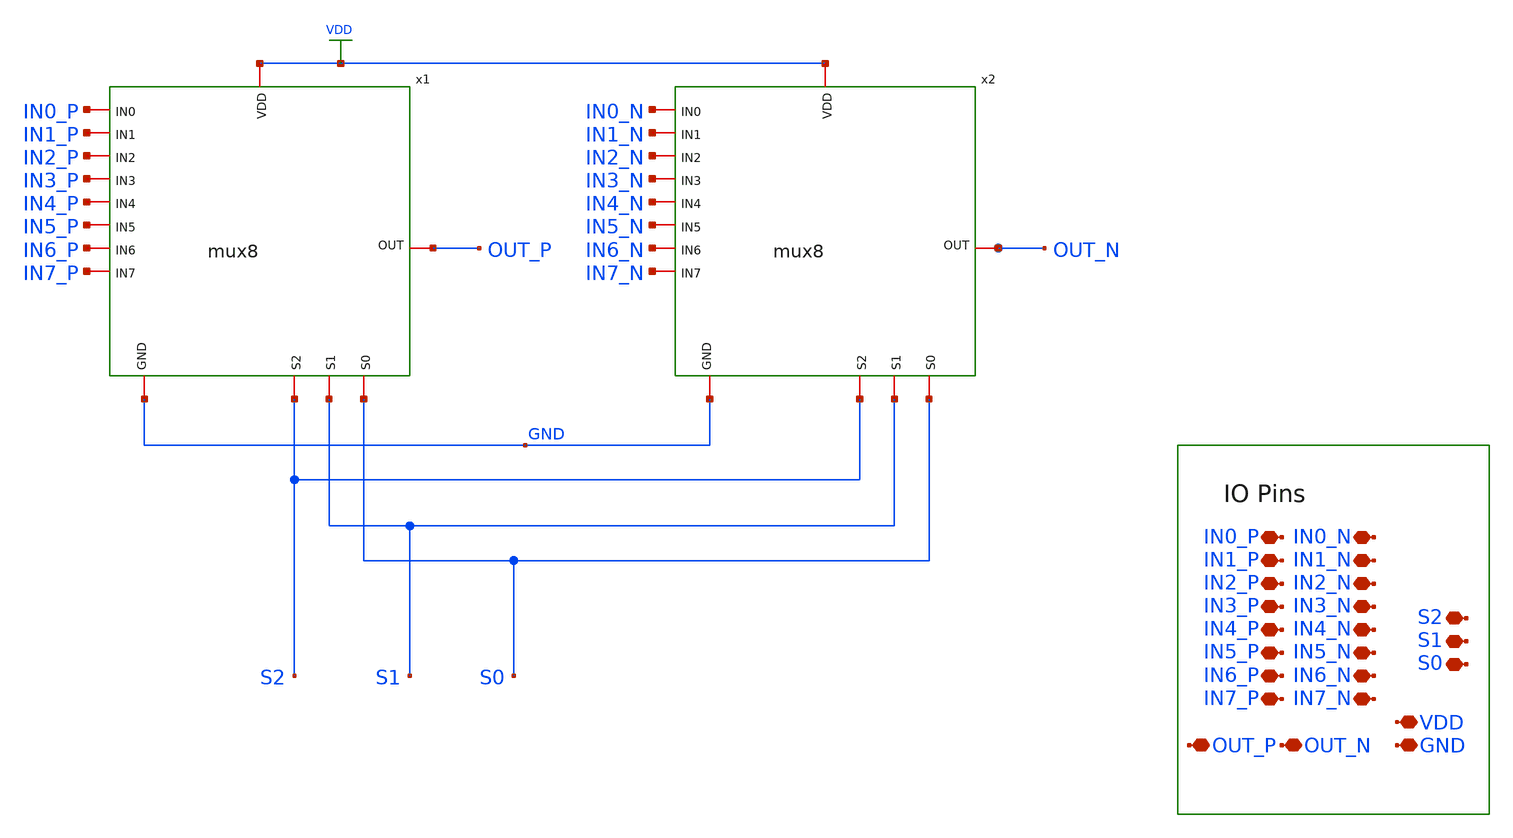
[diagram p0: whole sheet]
** sch_path: scope_sky130_v1/osc_input_mux.sch
**.subckt osc_input_mux IN1_P VDD GND IN2_P IN3_P IN4_P IN5_P IN6_P IN7_P IN0_P S2 S1 S0 OUT_P OUT_N
*+ IN1_N IN2_N IN3_N IN4_N IN5_N IN6_N IN7_N IN0_N
*.iopin IN1_P
*.iopin VDD
*.iopin GND
*.iopin IN2_P
*.iopin IN3_P
*.iopin IN4_P
*.iopin IN5_P
*.iopin IN6_P
*.iopin IN7_P
*.iopin IN0_P
*.iopin S2
*.iopin S1
*.iopin S0
*.iopin OUT_P
*.iopin OUT_N
*.iopin IN1_N
*.iopin IN2_N
*.iopin IN3_N
*.iopin IN4_N
*.iopin IN5_N
*.iopin IN6_N
*.iopin IN7_N
*.iopin IN0_N
x1 IN1_P IN2_P IN3_P IN4_P IN5_P IN6_P OUT_P IN7_P IN0_P S1 VDD S2 GND S0 mux8
x2 IN1_N IN2_N IN3_N IN4_N IN5_N IN6_N OUT_N IN7_N IN0_N S1 VDD S2 GND S0 mux8
**.ends

* expanding   symbol:  scope_sky130_v1/mux8.sym # of pins=14
** sym_path: scope_sky130_v1/mux8.sym
** sch_path: scope_sky130_v1/mux8.sch
.subckt mux8 IN1 IN2 IN3 IN4 IN5 IN6 OUT IN7 IN0 S1 VDD S2 GND S0
*.iopin IN3
*.iopin VDD
*.iopin GND
*.iopin S0
*.iopin OUT
*.iopin IN2
*.iopin IN1
*.iopin IN0
*.iopin S1
*.iopin IN7
*.iopin IN6
*.iopin IN5
*.iopin IN4
*.iopin S2
XM1 Sb S0 VDD VDD sky130_fd_pr__pfet_01v8_lvt L=0.35 W=1 nf=1 ad='int((1 + 1)/2) * 1 / 1 * 0.29' as='int((1 + 2)/2) * 1 / 1 * 0.29'
+ pd='2*int((1 + 1)/2) * (1 / 1 + 0.29)' ps='2*int((1 + 2)/2) * (1 / 1 + 0.29)' nrd='0.29 / 1 ' nrs='0.29 / 1 '
+ sa=0 sb=0 sd=0 mult=1 m=1
XM2 Sb S0 GND GND sky130_fd_pr__nfet_01v8_lvt L=0.15 W=1 nf=1 ad='int((1 + 1)/2) * 1 / 1 * 0.29' as='int((1 + 2)/2) * 1 / 1 * 0.29'
+ pd='2*int((1 + 1)/2) * (1 / 1 + 0.29)' ps='2*int((1 + 2)/2) * (1 / 1 + 0.29)' nrd='0.29 / 1 ' nrs='0.29 / 1 '
+ sa=0 sb=0 sd=0 mult=1 m=1
x1 IN7 net1 net5 S0 VDD GND tgate
x2 IN6 net1 net6 net5 VDD GND tgate
x3 IN5 net2 net5 net6 VDD GND tgate
x4 IN4 net2 S0 net5 VDD GND tgate
x5 IN3 net3 Sb S0 VDD GND tgate
x6 IN2 net3 S0 Sb VDD GND tgate
x7 IN1 net4 Sb S0 VDD GND tgate
x8 IN0 net4 S0 Sb VDD GND tgate
x9 net2 net1 S1 S2 net4 net3 OUT VDD GND mux4
.ends


* expanding   symbol:  scope_sky130_v1/tgate.sym # of pins=6
** sym_path: scope_sky130_v1/tgate.sym
** sch_path: scope_sky130_v1/tgate.sch
.subckt tgate IN OUT ENb EN VDD GND
*.iopin IN
*.iopin VDD
*.iopin GND
*.iopin ENb
*.iopin EN
*.iopin OUT
XM2 IN EN OUT GND sky130_fd_pr__nfet_01v8 L=0.15 W=0.5 nf=1 ad='int((1 + 1)/2) * 0.5 / 1 * 0.29' as='int((1 + 2)/2) * 0.5 / 1 * 0.29'
+ pd='2*int((1 + 1)/2) * (0.5 / 1 + 0.29)' ps='2*int((1 + 2)/2) * (0.5 / 1 + 0.29)' nrd='0.29 / 0.5 ' nrs='0.29 / 0.5 '
+ sa=0 sb=0 sd=0 mult=1 m=1
XM11 IN ENb OUT VDD sky130_fd_pr__pfet_01v8 L=0.15 W=0.5 nf=1 ad='int((nf+1)/2) * W/nf * 0.29' as='int((nf+2)/2) * W/nf * 0.29'
+ pd='2*int((nf+1)/2) * (W/nf + 0.29)' ps='2*int((nf+2)/2) * (W/nf + 0.29)' nrd='0.29 / W' nrs='0.29 / W'
+ sa=0 sb=0 sd=0 mult=1 m=1
.ends


* expanding   symbol:  scope_sky130_v1/mux4.sym # of pins=9
** sym_path: scope_sky130_v1/mux4.sym
** sch_path: scope_sky130_v1/mux4.sch
.subckt mux4 IN2 IN3 S0 S1 IN0 IN1 OUT VDD GND
*.iopin IN3
*.iopin VDD
*.iopin GND
*.iopin S0
*.iopin OUT
*.iopin IN2
*.iopin IN1
*.iopin IN0
*.iopin S1
XM1 Sb S0 VDD VDD sky130_fd_pr__pfet_01v8_lvt L=0.35 W=1 nf=1 ad='int((1 + 1)/2) * 1 / 1 * 0.29' as='int((1 + 2)/2) * 1 / 1 * 0.29'
+ pd='2*int((1 + 1)/2) * (1 / 1 + 0.29)' ps='2*int((1 + 2)/2) * (1 / 1 + 0.29)' nrd='0.29 / 1 ' nrs='0.29 / 1 '
+ sa=0 sb=0 sd=0 mult=1 m=1
XM2 Sb S0 GND GND sky130_fd_pr__nfet_01v8_lvt L=0.15 W=1 nf=1 ad='int((1 + 1)/2) * 1 / 1 * 0.29' as='int((1 + 2)/2) * 1 / 1 * 0.29'
+ pd='2*int((1 + 1)/2) * (1 / 1 + 0.29)' ps='2*int((1 + 2)/2) * (1 / 1 + 0.29)' nrd='0.29 / 1 ' nrs='0.29 / 1 '
+ sa=0 sb=0 sd=0 mult=1 m=1
x1 IN3 net1 Sb S0 VDD GND tgate
x2 IN2 net1 S0 Sb VDD GND tgate
x3 IN1 net2 Sb S0 VDD GND tgate
x4 IN0 net2 S0 Sb VDD GND tgate
x5 net2 net1 S1 OUT VDD GND mux2
.ends


* expanding   symbol:  scope_sky130_v1/mux2.sym # of pins=6
** sym_path: scope_sky130_v1/mux2.sym
** sch_path: scope_sky130_v1/mux2.sch
.subckt mux2 IN0 IN1 S OUT VDD GND
*.iopin IN1
*.iopin VDD
*.iopin GND
*.iopin S
*.iopin OUT
*.iopin IN0
XM1 Sb S VDD VDD sky130_fd_pr__pfet_01v8_lvt L=0.35 W=1 nf=1 ad='int((1 + 1)/2) * 1 / 1 * 0.29' as='int((1 + 2)/2) * 1 / 1 * 0.29'
+ pd='2*int((1 + 1)/2) * (1 / 1 + 0.29)' ps='2*int((1 + 2)/2) * (1 / 1 + 0.29)' nrd='0.29 / 1 ' nrs='0.29 / 1 '
+ sa=0 sb=0 sd=0 mult=1 m=1
XM2 Sb S GND GND sky130_fd_pr__nfet_01v8_lvt L=0.15 W=1 nf=1 ad='int((1 + 1)/2) * 1 / 1 * 0.29' as='int((1 + 2)/2) * 1 / 1 * 0.29'
+ pd='2*int((1 + 1)/2) * (1 / 1 + 0.29)' ps='2*int((1 + 2)/2) * (1 / 1 + 0.29)' nrd='0.29 / 1 ' nrs='0.29 / 1 '
+ sa=0 sb=0 sd=0 mult=1 m=1
x1 IN1 OUT Sb S VDD GND tgate
x2 IN0 OUT S Sb VDD GND tgate
.ends

.GLOBAL VDD
.end
